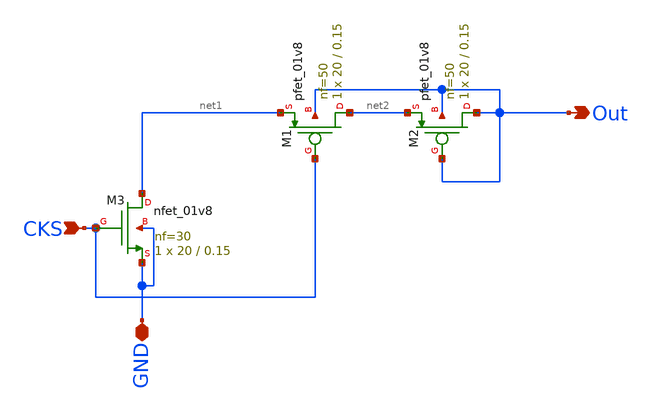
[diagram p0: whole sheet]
** sch_path: MN3test11111111.sch
**.subckt MN3test11111111 CKS GND Out
*.ipin CKS
*.iopin GND
*.opin Out
XM1 net2 CKS net1 Out sky130_fd_pr__pfet_01v8 L=0.15 W=20 nf=50 ad='int((nf+1)/2) * W/nf * 0.29' as='int((nf+2)/2) * W/nf * 0.29'
+ pd='2*int((nf+1)/2) * (W/nf + 0.29)' ps='2*int((nf+2)/2) * (W/nf + 0.29)' nrd='0.29 / W' nrs='0.29 / W'
+ sa=0 sb=0 sd=0 mult=1 m=1
XM2 Out Out net2 Out sky130_fd_pr__pfet_01v8 L=0.15 W=20 nf=50 ad='int((nf+1)/2) * W/nf * 0.29' as='int((nf+2)/2) * W/nf * 0.29'
+ pd='2*int((nf+1)/2) * (W/nf + 0.29)' ps='2*int((nf+2)/2) * (W/nf + 0.29)' nrd='0.29 / W' nrs='0.29 / W'
+ sa=0 sb=0 sd=0 mult=1 m=1
XM3 net1 CKS GND GND sky130_fd_pr__nfet_01v8 L=0.15 W=20 nf=30 ad='int((nf+1)/2) * W/nf * 0.29' as='int((nf+2)/2) * W/nf * 0.29'
+ pd='2*int((nf+1)/2) * (W/nf + 0.29)' ps='2*int((nf+2)/2) * (W/nf + 0.29)' nrd='0.29 / W' nrs='0.29 / W'
+ sa=0 sb=0 sd=0 mult=1 m=1
**.ends
.end
